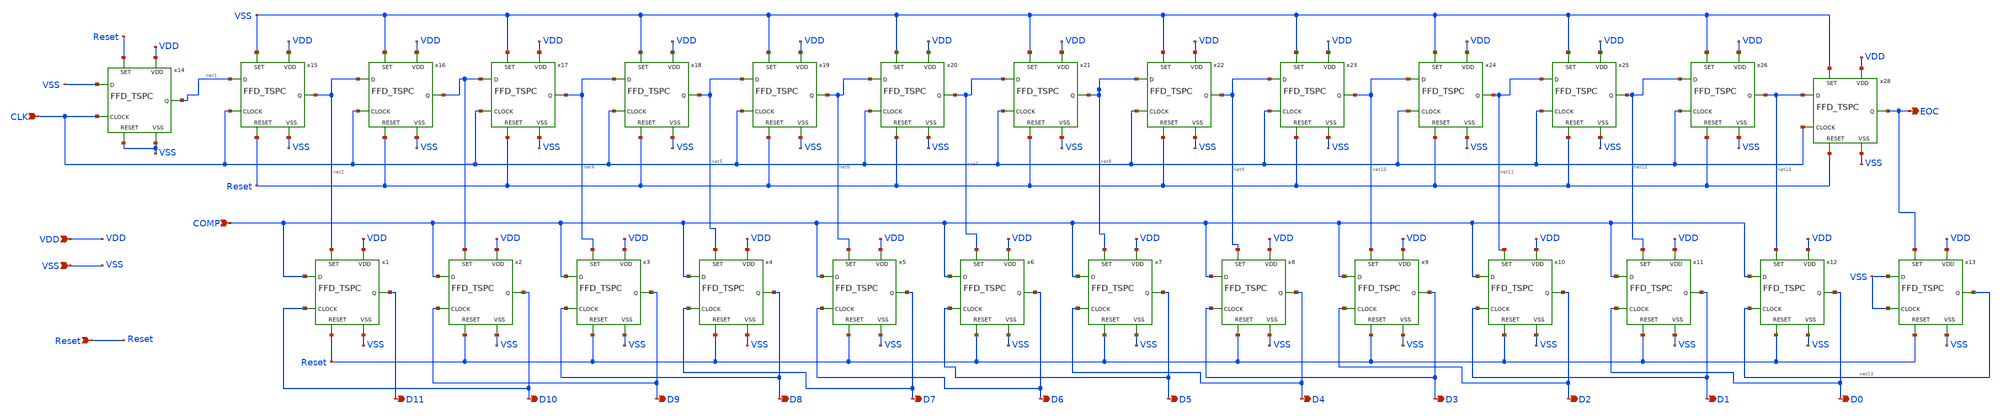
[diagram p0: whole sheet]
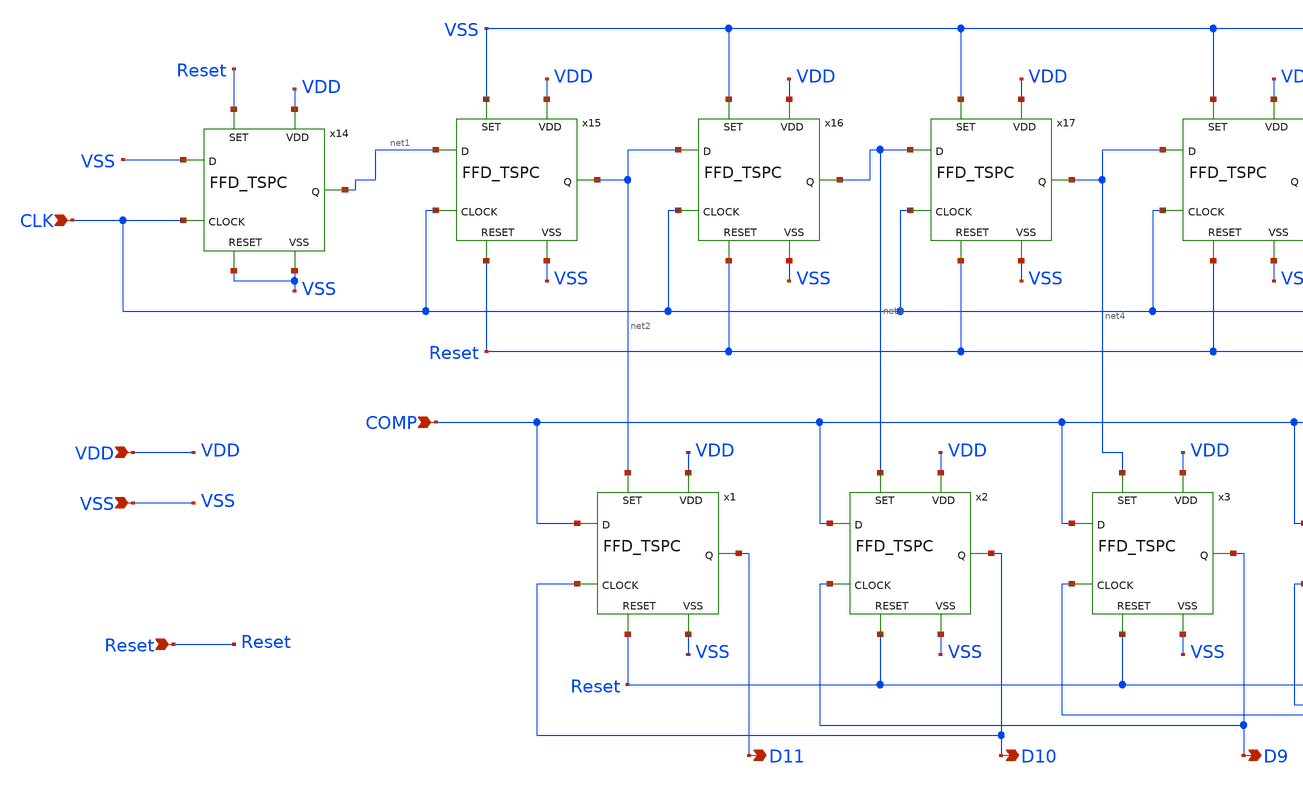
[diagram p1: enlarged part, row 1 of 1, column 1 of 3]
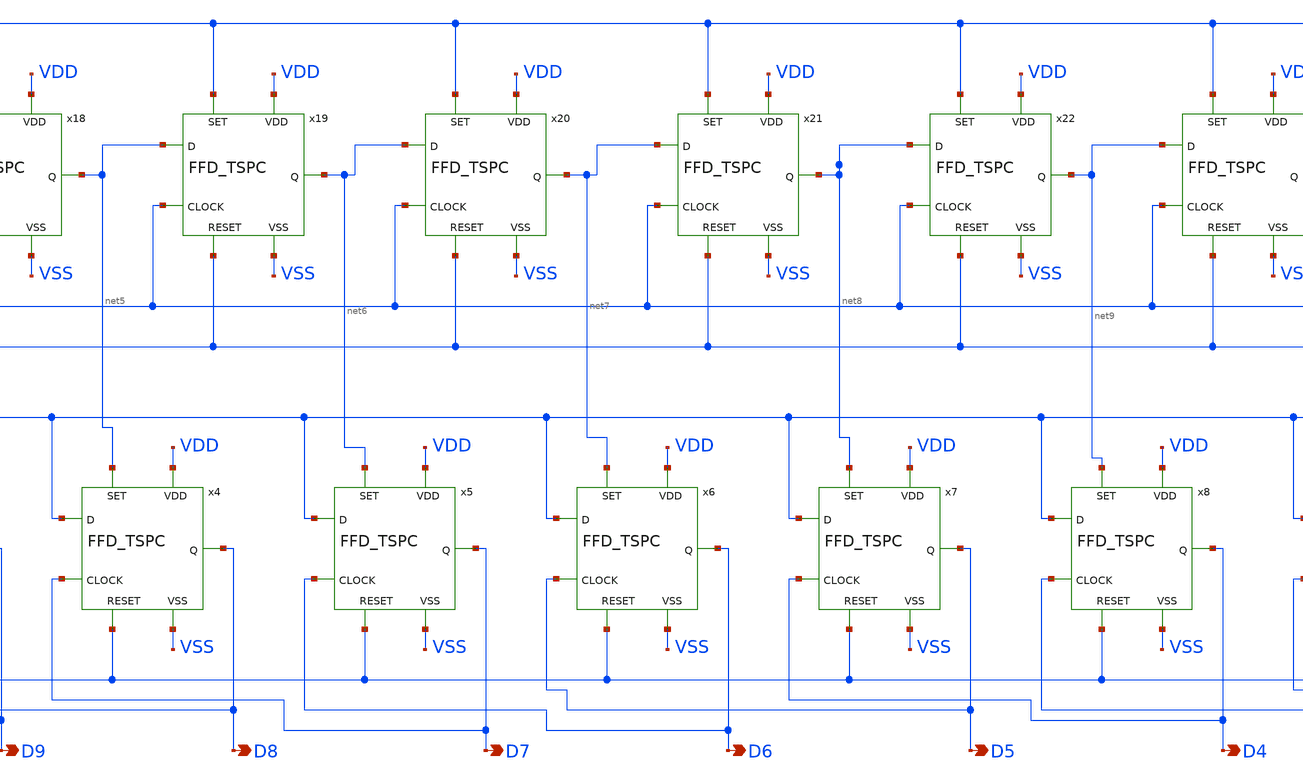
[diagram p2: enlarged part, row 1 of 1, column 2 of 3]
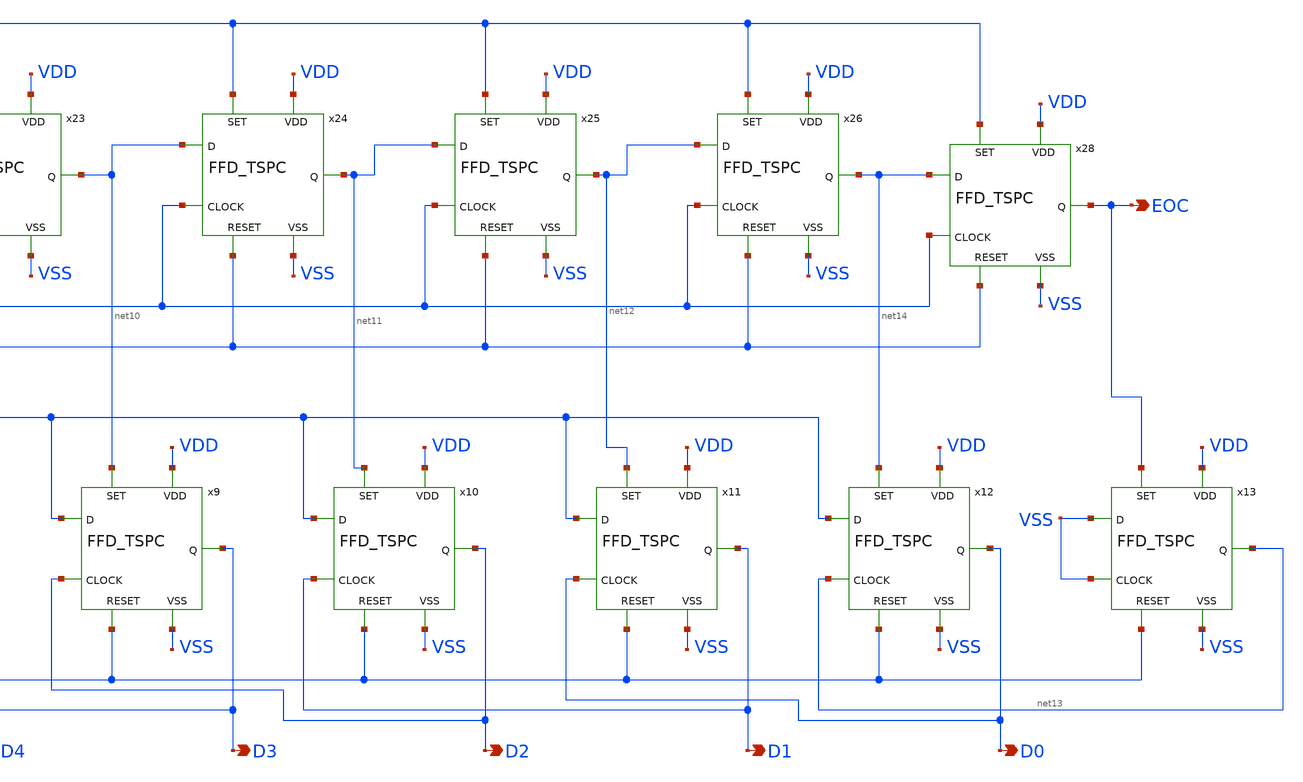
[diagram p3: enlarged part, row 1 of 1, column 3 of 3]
** sch_path: SAR_Logic_TSPC.sch
**.subckt SAR_Logic_TSPC CLK VDD VSS COMP D11 D10 D9 D8 D7 D6 D5 D4 D3 D2 D1 D0 Reset EOC
*.ipin CLK
*.ipin VDD
*.ipin VSS
*.ipin COMP
*.opin D11
*.opin D10
*.opin D9
*.opin D8
*.opin D7
*.opin D6
*.opin D5
*.opin D4
*.opin D3
*.opin D2
*.opin D1
*.opin D0
*.ipin Reset
*.opin EOC
x1 VDD VSS net2 D10 Reset COMP D11 FFD_TSPC
x2 VDD VSS net3 D9 Reset COMP D10 FFD_TSPC
x3 VDD VSS net4 D8 Reset COMP D9 FFD_TSPC
x4 VDD VSS net5 D7 Reset COMP D8 FFD_TSPC
x5 VDD VSS net6 D6 Reset COMP D7 FFD_TSPC
x6 VDD VSS net7 D5 Reset COMP D6 FFD_TSPC
x7 VDD VSS net8 D4 Reset COMP D5 FFD_TSPC
x8 VDD VSS net9 D3 Reset COMP D4 FFD_TSPC
x9 VDD VSS net10 D2 Reset COMP D3 FFD_TSPC
x10 VDD VSS net11 D1 Reset COMP D2 FFD_TSPC
x11 VDD VSS net12 D0 Reset COMP D1 FFD_TSPC
x12 VDD VSS net14 net13 Reset COMP D0 FFD_TSPC
x13 VDD VSS EOC VSS Reset VSS net13 FFD_TSPC
x14 VDD VSS Reset CLK VSS VSS net1 FFD_TSPC
x15 VDD VSS VSS CLK Reset net1 net2 FFD_TSPC
x16 VDD VSS VSS CLK Reset net2 net3 FFD_TSPC
x17 VDD VSS VSS CLK Reset net3 net4 FFD_TSPC
x18 VDD VSS VSS CLK Reset net4 net5 FFD_TSPC
x19 VDD VSS VSS CLK Reset net5 net6 FFD_TSPC
x20 VDD VSS VSS CLK Reset net6 net7 FFD_TSPC
x21 VDD VSS VSS CLK Reset net7 net8 FFD_TSPC
x22 VDD VSS VSS CLK Reset net8 net9 FFD_TSPC
x23 VDD VSS VSS CLK Reset net9 net10 FFD_TSPC
x24 VDD VSS VSS CLK Reset net10 net11 FFD_TSPC
x25 VDD VSS VSS CLK Reset net11 net12 FFD_TSPC
x26 VDD VSS VSS CLK Reset net12 net14 FFD_TSPC
x28 VDD VSS VSS CLK Reset net14 EOC FFD_TSPC
**.ends

* expanding   symbol:  FFD_TSPC.sym # of pins=7
** sym_path: FFD_TSPC.sym
** sch_path: FFD_TSPC.sch
.subckt FFD_TSPC VDD VSS SET CLOCK RESET D Q
*.ipin CLOCK
*.ipin SET
*.ipin RESET
*.ipin VDD
*.ipin VSS
*.ipin D
*.opin Q
XM1 net2 D VSS VSS sky130_fd_pr__nfet_01v8 L=0.15 W=0.5 nf=1 ad='int((nf+1)/2) * W/nf * 0.29' as='int((nf+2)/2) * W/nf * 0.29'
+ pd='2*int((nf+1)/2) * (W/nf + 0.29)' ps='2*int((nf+2)/2) * (W/nf + 0.29)' nrd='0.29 / W' nrs='0.29 / W'
+ sa=0 sb=0 sd=0 mult=1 m=1
XM2 net3 CLOCK VSS VSS sky130_fd_pr__nfet_01v8 L=0.15 W=0.5 nf=1 ad='int((nf+1)/2) * W/nf * 0.29' as='int((nf+2)/2) * W/nf * 0.29'
+ pd='2*int((nf+1)/2) * (W/nf + 0.29)' ps='2*int((nf+2)/2) * (W/nf + 0.29)' nrd='0.29 / W' nrs='0.29 / W'
+ sa=0 sb=0 sd=0 mult=1 m=1
XM3 net4 Q_pre VSS VSS sky130_fd_pr__nfet_01v8 L=0.15 W=0.5 nf=1 ad='int((nf+1)/2) * W/nf * 0.29' as='int((nf+2)/2) * W/nf * 0.29'
+ pd='2*int((nf+1)/2) * (W/nf + 0.29)' ps='2*int((nf+2)/2) * (W/nf + 0.29)' nrd='0.29 / W' nrs='0.29 / W'
+ sa=0 sb=0 sd=0 mult=1 m=1
XM4 net2 CLOCK net1 VDD sky130_fd_pr__pfet_01v8 L=0.15 W=2 nf=1 ad='int((nf+1)/2) * W/nf * 0.29' as='int((nf+2)/2) * W/nf * 0.29'
+ pd='2*int((nf+1)/2) * (W/nf + 0.29)' ps='2*int((nf+2)/2) * (W/nf + 0.29)' nrd='0.29 / W' nrs='0.29 / W'
+ sa=0 sb=0 sd=0 mult=1 m=1
XM5 Q_pre net2 net3 VSS sky130_fd_pr__nfet_01v8 L=0.15 W=0.5 nf=1 ad='int((nf+1)/2) * W/nf * 0.29' as='int((nf+2)/2) * W/nf * 0.29'
+ pd='2*int((nf+1)/2) * (W/nf + 0.29)' ps='2*int((nf+2)/2) * (W/nf + 0.29)' nrd='0.29 / W' nrs='0.29 / W'
+ sa=0 sb=0 sd=0 mult=1 m=1
XM6 QB_pre CLOCK net4 VSS sky130_fd_pr__nfet_01v8 L=0.15 W=0.5 nf=1 ad='int((nf+1)/2) * W/nf * 0.29'
+ as='int((nf+2)/2) * W/nf * 0.29' pd='2*int((nf+1)/2) * (W/nf + 0.29)' ps='2*int((nf+2)/2) * (W/nf + 0.29)'
+ nrd='0.29 / W' nrs='0.29 / W' sa=0 sb=0 sd=0 mult=1 m=1
XM7 Q QB_pre VSS VSS sky130_fd_pr__nfet_01v8 L=0.15 W=3 nf=1 ad='int((nf+1)/2) * W/nf * 0.29' as='int((nf+2)/2) * W/nf * 0.29'
+ pd='2*int((nf+1)/2) * (W/nf + 0.29)' ps='2*int((nf+2)/2) * (W/nf + 0.29)' nrd='0.29 / W' nrs='0.29 / W'
+ sa=0 sb=0 sd=0 mult=1 m=1
XM8 net1 D VDD VDD sky130_fd_pr__pfet_01v8 L=0.15 W=2 nf=1 ad='int((nf+1)/2) * W/nf * 0.29' as='int((nf+2)/2) * W/nf * 0.29'
+ pd='2*int((nf+1)/2) * (W/nf + 0.29)' ps='2*int((nf+2)/2) * (W/nf + 0.29)' nrd='0.29 / W' nrs='0.29 / W'
+ sa=0 sb=0 sd=0 mult=1 m=1
XM9 Q_pre CLOCK VDD VDD sky130_fd_pr__pfet_01v8 L=0.15 W=2 nf=1 ad='int((nf+1)/2) * W/nf * 0.29' as='int((nf+2)/2) * W/nf * 0.29'
+ pd='2*int((nf+1)/2) * (W/nf + 0.29)' ps='2*int((nf+2)/2) * (W/nf + 0.29)' nrd='0.29 / W' nrs='0.29 / W'
+ sa=0 sb=0 sd=0 mult=1 m=1
XM10 net5 Q_pre VDD VDD sky130_fd_pr__pfet_01v8 L=0.15 W=2 nf=1 ad='int((nf+1)/2) * W/nf * 0.29' as='int((nf+2)/2) * W/nf * 0.29'
+ pd='2*int((nf+1)/2) * (W/nf + 0.29)' ps='2*int((nf+2)/2) * (W/nf + 0.29)' nrd='0.29 / W' nrs='0.29 / W'
+ sa=0 sb=0 sd=0 mult=1 m=1
XM11 QB_pre RS VDD VDD sky130_fd_pr__pfet_01v8 L=0.15 W=2 nf=1 ad='int((nf+1)/2) * W/nf * 0.29' as='int((nf+2)/2) * W/nf * 0.29'
+ pd='2*int((nf+1)/2) * (W/nf + 0.29)' ps='2*int((nf+2)/2) * (W/nf + 0.29)' nrd='0.29 / W' nrs='0.29 / W'
+ sa=0 sb=0 sd=0 mult=1 m=1
XM12 Q QB_pre VDD VDD sky130_fd_pr__pfet_01v8 L=0.15 W=6 nf=1 ad='int((nf+1)/2) * W/nf * 0.29' as='int((nf+2)/2) * W/nf * 0.29'
+ pd='2*int((nf+1)/2) * (W/nf + 0.29)' ps='2*int((nf+2)/2) * (W/nf + 0.29)' nrd='0.29 / W' nrs='0.29 / W'
+ sa=0 sb=0 sd=0 mult=1 m=1
XM13 QB_pre SET VSS VSS sky130_fd_pr__nfet_01v8 L=0.15 W=0.5 nf=1 ad='int((nf+1)/2) * W/nf * 0.29' as='int((nf+2)/2) * W/nf * 0.29'
+ pd='2*int((nf+1)/2) * (W/nf + 0.29)' ps='2*int((nf+2)/2) * (W/nf + 0.29)' nrd='0.29 / W' nrs='0.29 / W'
+ sa=0 sb=0 sd=0 mult=1 m=1
x1 VDD RESET RS VSS Inverter
XM14 QB_pre SET net5 VDD sky130_fd_pr__pfet_01v8 L=0.15 W=2 nf=1 ad='int((nf+1)/2) * W/nf * 0.29' as='int((nf+2)/2) * W/nf * 0.29'
+ pd='2*int((nf+1)/2) * (W/nf + 0.29)' ps='2*int((nf+2)/2) * (W/nf + 0.29)' nrd='0.29 / W' nrs='0.29 / W'
+ sa=0 sb=0 sd=0 mult=1 m=1
.ends


* expanding   symbol:  Inverter.sym # of pins=4
** sym_path: Inverter.sym
** sch_path: Inverter.sch
.subckt Inverter VDD IN OUT VSS
*.ipin IN
*.ipin VSS
*.ipin VDD
*.opin OUT
XM1 OUT IN VSS VSS sky130_fd_pr__nfet_01v8 L=0.3 W=1 nf=1 ad='int((nf+1)/2) * W/nf * 0.29' as='int((nf+2)/2) * W/nf * 0.29'
+ pd='2*int((nf+1)/2) * (W/nf + 0.29)' ps='2*int((nf+2)/2) * (W/nf + 0.29)' nrd='0.29 / W' nrs='0.29 / W'
+ sa=0 sb=0 sd=0 mult=1 m=1
XM2 OUT IN VDD VDD sky130_fd_pr__pfet_01v8 L=0.3 W=2 nf=1 ad='int((nf+1)/2) * W/nf * 0.29' as='int((nf+2)/2) * W/nf * 0.29'
+ pd='2*int((nf+1)/2) * (W/nf + 0.29)' ps='2*int((nf+2)/2) * (W/nf + 0.29)' nrd='0.29 / W' nrs='0.29 / W'
+ sa=0 sb=0 sd=0 mult=1 m=1
.ends

.end
